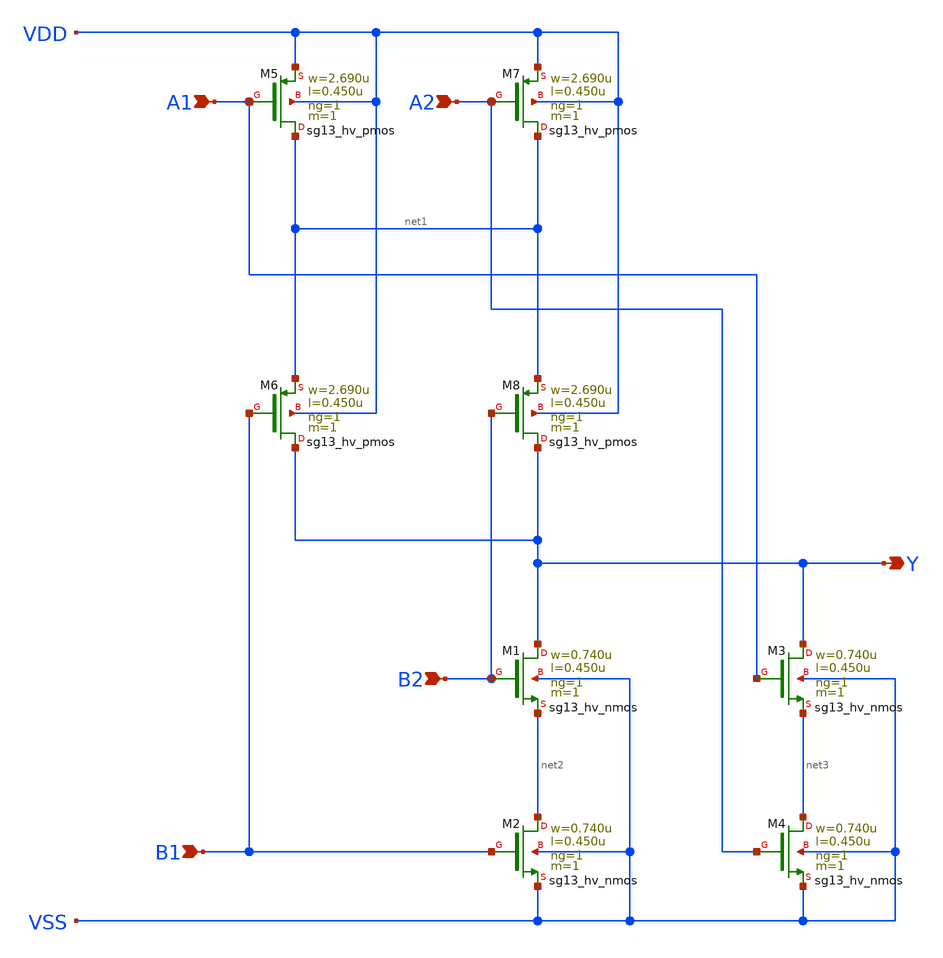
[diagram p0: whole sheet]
** sch_path: ihp-sg13g2/libs.ref/sg13g2_stdcell_hv/sch/xschem/sg13g2_hv_a22oi_1.sch
* Copyright 2023 IHP PDK Authors
* Licensed under the Apache License, Version 2.0 (the "License");
* you may not use this file except in compliance with the License.
* You may obtain a copy of the License at
* https://www.apache.org/licenses/LICENSE-2.0
* Unless required by applicable law or agreed to in writing, software
* distributed under the License is distributed on an "AS IS" BASIS,
* WITHOUT WARRANTIES OR CONDITIONS OF ANY KIND, either express or implied.
* See the License for the specific language governing permissions and
* limitations under the License.
**.subckt sg13g2_hv_a22oi_1 A1 A2 B1 Y B2
*.ipin A1
*.ipin A2
*.ipin B1
*.opin Y
*.ipin B2
XM1 Y B2 net2 VSS sg13_hv_nmos w=0.740u l=0.450u ng=1 m=1 mm_ok=1
XM2 net2 B1 VSS VSS sg13_hv_nmos w=0.740u l=0.450u ng=1 m=1 mm_ok=1
XM3 Y A1 net3 VSS sg13_hv_nmos w=0.740u l=0.450u ng=1 m=1 mm_ok=1
XM4 net3 A2 VSS VSS sg13_hv_nmos w=0.740u l=0.450u ng=1 m=1 mm_ok=1
XM5 net1 A1 VDD VDD sg13_hv_pmos w=2.690u l=0.450u ng=1 m=1 mm_ok=1
XM6 Y B1 net1 VDD sg13_hv_pmos w=2.690u l=0.450u ng=1 m=1 mm_ok=1
XM7 net1 A2 VDD VDD sg13_hv_pmos w=2.690u l=0.450u ng=1 m=1 mm_ok=1
XM8 Y B2 net1 VDD sg13_hv_pmos w=2.690u l=0.450u ng=1 m=1 mm_ok=1
**.ends
.end
